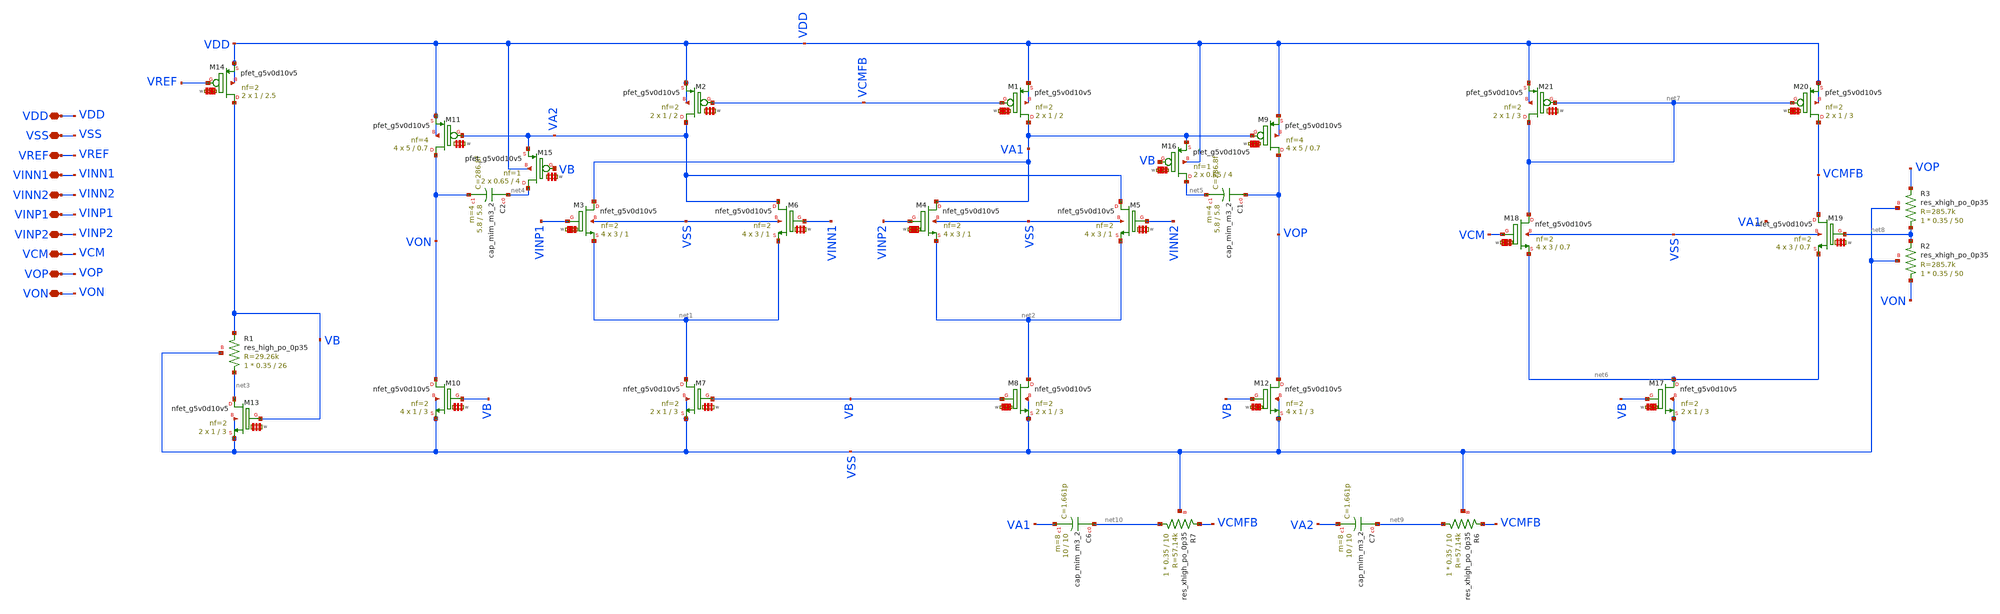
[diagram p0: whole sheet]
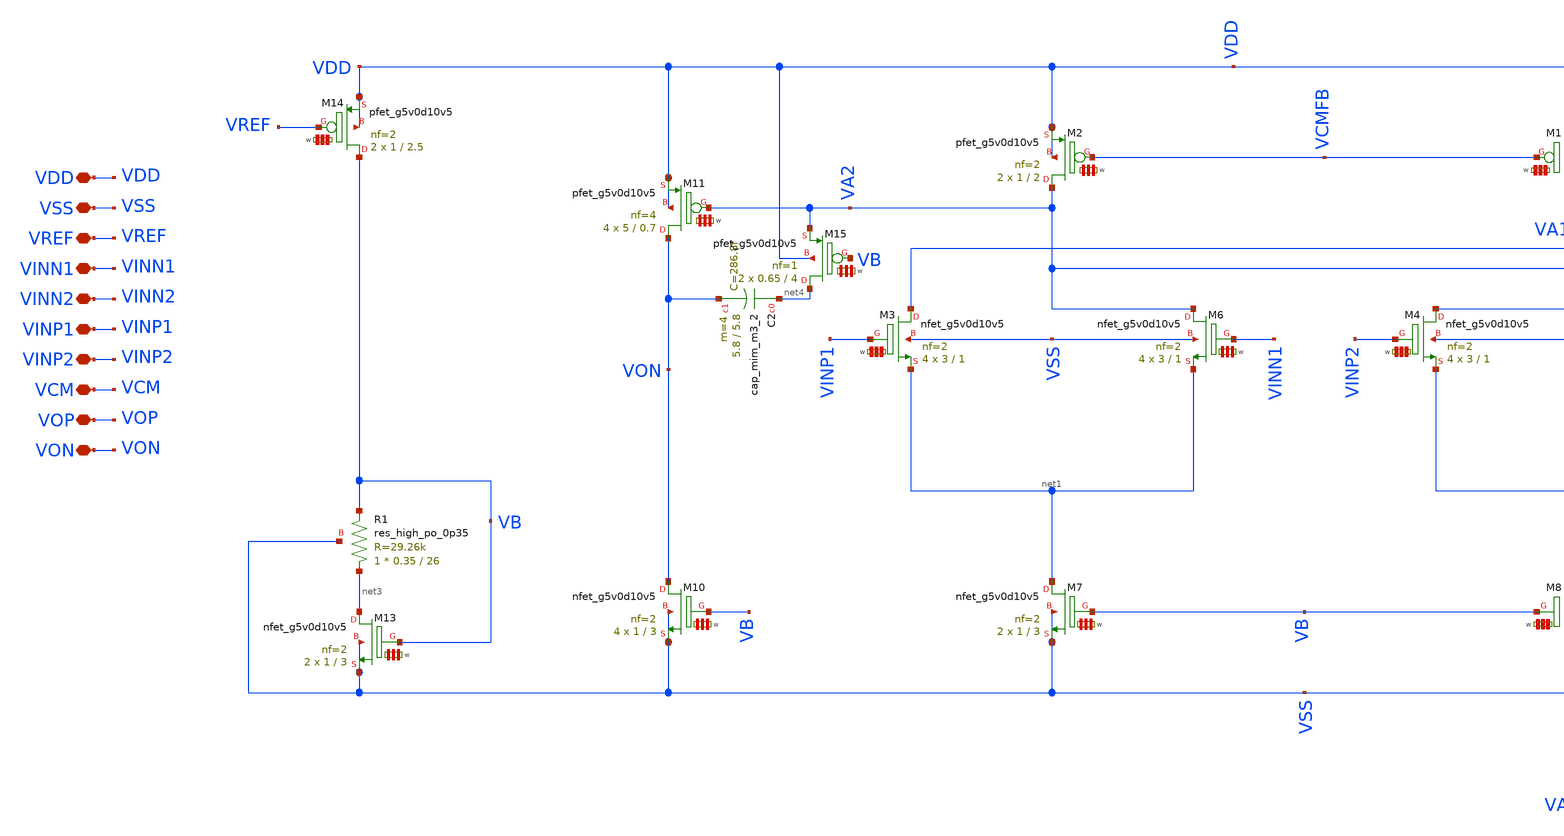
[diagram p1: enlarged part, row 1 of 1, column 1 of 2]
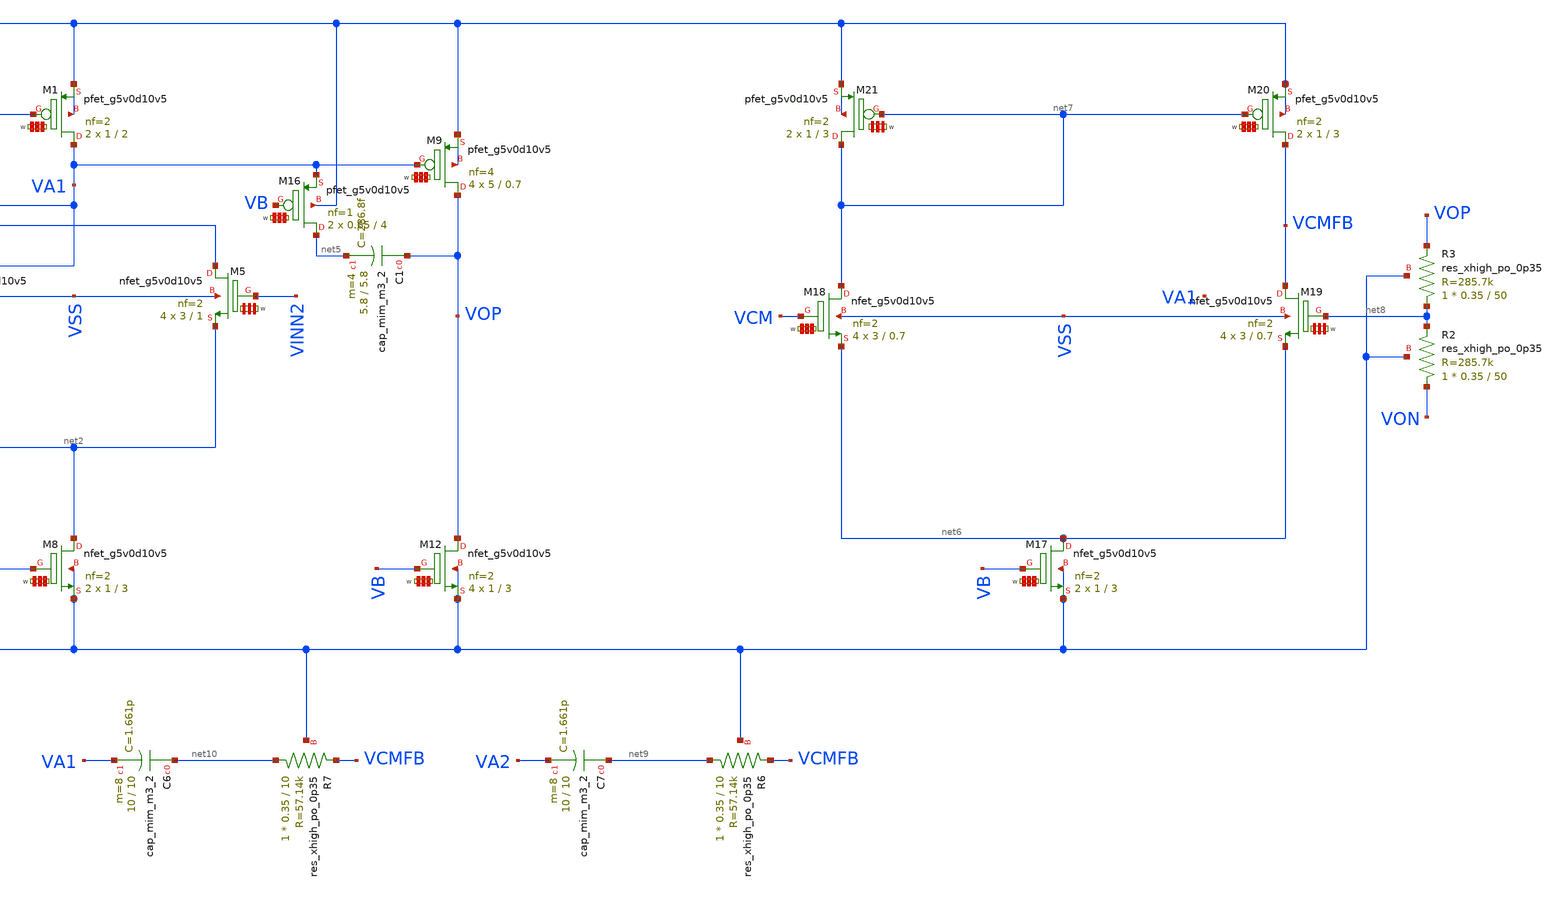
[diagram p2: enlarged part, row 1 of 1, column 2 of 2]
** sch_path: LIB/Sky130A/DDA/DDA002_NMOS_sky130_5V.sch
**.subckt DDA002_NMOS_sky130_5V VDD VSS VREF VINN1 VINN2 VINP1 VINP2 VCM VOP VON
*.iopin VDD
*.iopin VSS
*.iopin VREF
*.iopin VINN1
*.iopin VINN2
*.iopin VINP1
*.iopin VINP2
*.iopin VCM
*.iopin VOP
*.iopin VON
XM2 VA2 VCMFB VDD VDD sky130_fd_pr__pfet_g5v0d10v5 L=2 W='1 * 2 ' nf=2 ad='int((2 + 1)/2) * 1 * 0.29'
+ as='int((2 + 2)/2) * 1 * 0.29' pd='2*int((2 + 1)/2) * (1 + 0.29)' ps='2*int((2 + 2)/2) * (1 + 0.29)'
+ nrd='0.29 / 1 / 2 ' nrs='0.29 / 1 / 2 ' sa=0 sb=0 sd=0 mult=2 m=2
XM3 VA1 VINP1 net1 VSS sky130_fd_pr__nfet_g5v0d10v5 L=1 W='3 * 2 ' nf=2 ad='int((nf+1)/2) * W / nf * 0.29'
+ as='int((nf+2)/2) * W / nf * 0.29' pd='2*int((nf+1)/2) * (W / nf + 0.29)' ps='2*int((nf+2)/2) * (W / nf + 0.29)'
+ nrd='0.29 / W ' nrs='0.29 / W ' sa=0 sb=0 sd=0 mult=4 m=4
XM13 net3 VB VSS VSS sky130_fd_pr__nfet_g5v0d10v5 L=3 W='1 * 2 ' nf=2 ad='int((nf+1)/2) * W / nf * 0.29'
+ as='int((nf+2)/2) * W / nf * 0.29' pd='2*int((nf+1)/2) * (W / nf + 0.29)' ps='2*int((nf+2)/2) * (W / nf + 0.29)'
+ nrd='0.29 / W ' nrs='0.29 / W ' sa=0 sb=0 sd=0 mult=2 m=2
XR1 net3 VB VSS sky130_fd_pr__res_high_po_0p35 L=26 mult=1 m=1
XM14 VB VREF VDD VDD sky130_fd_pr__pfet_g5v0d10v5 L=2.5 W='1 * 2 ' nf=2 ad='int((2 + 1)/2) * 1 * 0.29'
+ as='int((2 + 2)/2) * 1 * 0.29' pd='2*int((2 + 1)/2) * (1 + 0.29)' ps='2*int((2 + 2)/2) * (1 + 0.29)'
+ nrd='0.29 / 1 / 2 ' nrs='0.29 / 1 / 2 ' sa=0 sb=0 sd=0 mult=2 m=2
XM7 net1 VB VSS VSS sky130_fd_pr__nfet_g5v0d10v5 L=3 W='1 * 2 ' nf=2 ad='int((nf+1)/2) * W / nf * 0.29'
+ as='int((nf+2)/2) * W / nf * 0.29' pd='2*int((nf+1)/2) * (W / nf + 0.29)' ps='2*int((nf+2)/2) * (W / nf + 0.29)'
+ nrd='0.29 / W ' nrs='0.29 / W ' sa=0 sb=0 sd=0 mult=2 m=2
XM8 net2 VB VSS VSS sky130_fd_pr__nfet_g5v0d10v5 L=3 W='1 * 2 ' nf=2 ad='int((nf+1)/2) * W / nf * 0.29'
+ as='int((nf+2)/2) * W / nf * 0.29' pd='2*int((nf+1)/2) * (W / nf + 0.29)' ps='2*int((nf+2)/2) * (W / nf + 0.29)'
+ nrd='0.29 / W ' nrs='0.29 / W ' sa=0 sb=0 sd=0 mult=2 m=2
XM10 VON VB VSS VSS sky130_fd_pr__nfet_g5v0d10v5 L=3 W='1 * 2 ' nf=2 ad='int((nf+1)/2) * W / nf * 0.29'
+ as='int((nf+2)/2) * W / nf * 0.29' pd='2*int((nf+1)/2) * (W / nf + 0.29)' ps='2*int((nf+2)/2) * (W / nf + 0.29)'
+ nrd='0.29 / W ' nrs='0.29 / W ' sa=0 sb=0 sd=0 mult=4 m=4
XM12 VOP VB VSS VSS sky130_fd_pr__nfet_g5v0d10v5 L=3 W='1 * 2 ' nf=2 ad='int((nf+1)/2) * W / nf * 0.29'
+ as='int((nf+2)/2) * W / nf * 0.29' pd='2*int((nf+1)/2) * (W / nf + 0.29)' ps='2*int((nf+2)/2) * (W / nf + 0.29)'
+ nrd='0.29 / W ' nrs='0.29 / W ' sa=0 sb=0 sd=0 mult=4 m=4
XM1 VA1 VCMFB VDD VDD sky130_fd_pr__pfet_g5v0d10v5 L=2 W='1 * 2 ' nf=2 ad='int((2 + 1)/2) * 1 * 0.29'
+ as='int((2 + 2)/2) * 1 * 0.29' pd='2*int((2 + 1)/2) * (1 + 0.29)' ps='2*int((2 + 2)/2) * (1 + 0.29)'
+ nrd='0.29 / 1 / 2 ' nrs='0.29 / 1 / 2 ' sa=0 sb=0 sd=0 mult=2 m=2
XM6 VA2 VINN1 net1 VSS sky130_fd_pr__nfet_g5v0d10v5 L=1 W='3 * 2 ' nf=2 ad='int((nf+1)/2) * W / nf * 0.29'
+ as='int((nf+2)/2) * W / nf * 0.29' pd='2*int((nf+1)/2) * (W / nf + 0.29)' ps='2*int((nf+2)/2) * (W / nf + 0.29)'
+ nrd='0.29 / W ' nrs='0.29 / W ' sa=0 sb=0 sd=0 mult=4 m=4
XM5 VA2 VINN2 net2 VSS sky130_fd_pr__nfet_g5v0d10v5 L=1 W='3 * 2 ' nf=2 ad='int((nf+1)/2) * W / nf * 0.29'
+ as='int((nf+2)/2) * W / nf * 0.29' pd='2*int((nf+1)/2) * (W / nf + 0.29)' ps='2*int((nf+2)/2) * (W / nf + 0.29)'
+ nrd='0.29 / W ' nrs='0.29 / W ' sa=0 sb=0 sd=0 mult=4 m=4
XM4 VA1 VINP2 net2 VSS sky130_fd_pr__nfet_g5v0d10v5 L=1 W='3 * 2 ' nf=2 ad='int((nf+1)/2) * W / nf * 0.29'
+ as='int((nf+2)/2) * W / nf * 0.29' pd='2*int((nf+1)/2) * (W / nf + 0.29)' ps='2*int((nf+2)/2) * (W / nf + 0.29)'
+ nrd='0.29 / W ' nrs='0.29 / W ' sa=0 sb=0 sd=0 mult=4 m=4
XM9 VOP VA1 VDD VDD sky130_fd_pr__pfet_g5v0d10v5 L=0.7 W='5 * 4 ' nf=4 ad='int((4 + 1)/2) * 5 * 0.29'
+ as='int((4 + 2)/2) * 5 * 0.29' pd='2*int((4 + 1)/2) * (5 + 0.29)' ps='2*int((4 + 2)/2) * (5 + 0.29)'
+ nrd='0.29 / 5 / 4 ' nrs='0.29 / 5 / 4 ' sa=0 sb=0 sd=0 mult=4 m=4
XM11 VON VA2 VDD VDD sky130_fd_pr__pfet_g5v0d10v5 L=0.7 W='5 * 4 ' nf=4 ad='int((4 + 1)/2) * 5 * 0.29'
+ as='int((4 + 2)/2) * 5 * 0.29' pd='2*int((4 + 1)/2) * (5 + 0.29)' ps='2*int((4 + 2)/2) * (5 + 0.29)'
+ nrd='0.29 / 5 / 4 ' nrs='0.29 / 5 / 4 ' sa=0 sb=0 sd=0 mult=4 m=4
XC2 net4 VON sky130_fd_pr__cap_mim_m3_2 W=5.8 L=5.8 MF=4 m=4
XM15 net4 VB VA2 VDD sky130_fd_pr__pfet_g5v0d10v5 L=4 W='0.65 * 1 ' nf=1 ad='int((1 + 1)/2) * 0.65 * 0.29'
+ as='int((1 + 2)/2) * 0.65 * 0.29' pd='2*int((1 + 1)/2) * (0.65 + 0.29)' ps='2*int((1 + 2)/2) * (0.65 + 0.29)'
+ nrd='0.29 / 0.65 / 1 ' nrs='0.29 / 0.65 / 1 ' sa=0 sb=0 sd=0 mult=2 m=2
XM17 net6 VB VSS VSS sky130_fd_pr__nfet_g5v0d10v5 L=3 W='1 * 2 ' nf=2 ad='int((nf+1)/2) * W / nf * 0.29'
+ as='int((nf+2)/2) * W / nf * 0.29' pd='2*int((nf+1)/2) * (W / nf + 0.29)' ps='2*int((nf+2)/2) * (W / nf + 0.29)'
+ nrd='0.29 / W ' nrs='0.29 / W ' sa=0 sb=0 sd=0 mult=2 m=2
XM18 net7 VCM net6 VSS sky130_fd_pr__nfet_g5v0d10v5 L=0.7 W='3 * 2 ' nf=2 ad='int((nf+1)/2) * W / nf * 0.29'
+ as='int((nf+2)/2) * W / nf * 0.29' pd='2*int((nf+1)/2) * (W / nf + 0.29)' ps='2*int((nf+2)/2) * (W / nf + 0.29)'
+ nrd='0.29 / W ' nrs='0.29 / W ' sa=0 sb=0 sd=0 mult=4 m=4
XM19 VCMFB net8 net6 VSS sky130_fd_pr__nfet_g5v0d10v5 L=0.7 W='3 * 2 ' nf=2 ad='int((nf+1)/2) * W / nf * 0.29'
+ as='int((nf+2)/2) * W / nf * 0.29' pd='2*int((nf+1)/2) * (W / nf + 0.29)' ps='2*int((nf+2)/2) * (W / nf + 0.29)'
+ nrd='0.29 / W ' nrs='0.29 / W ' sa=0 sb=0 sd=0 mult=4 m=4
XM21 net7 net7 VDD VDD sky130_fd_pr__pfet_g5v0d10v5 L=3 W='1 * 2 ' nf=2 ad='int((2 + 1)/2) * 1 * 0.29'
+ as='int((2 + 2)/2) * 1 * 0.29' pd='2*int((2 + 1)/2) * (1 + 0.29)' ps='2*int((2 + 2)/2) * (1 + 0.29)'
+ nrd='0.29 / 1 / 2 ' nrs='0.29 / 1 / 2 ' sa=0 sb=0 sd=0 mult=2 m=2
XM20 VCMFB net7 VDD VDD sky130_fd_pr__pfet_g5v0d10v5 L=3 W='1 * 2 ' nf=2 ad='int((2 + 1)/2) * 1 * 0.29'
+ as='int((2 + 2)/2) * 1 * 0.29' pd='2*int((2 + 1)/2) * (1 + 0.29)' ps='2*int((2 + 2)/2) * (1 + 0.29)'
+ nrd='0.29 / 1 / 2 ' nrs='0.29 / 1 / 2 ' sa=0 sb=0 sd=0 mult=2 m=2
XC6 net10 VA1 sky130_fd_pr__cap_mim_m3_2 W=10 L=10 MF=8 m=8
XR7 net10 VCMFB VSS sky130_fd_pr__res_xhigh_po_0p35 L=10 mult=1 m=1
XC7 net9 VA2 sky130_fd_pr__cap_mim_m3_2 W=10 L=10 MF=8 m=8
XR6 net9 VCMFB VSS sky130_fd_pr__res_xhigh_po_0p35 L=10 mult=1 m=1
XR2 VON net8 VSS sky130_fd_pr__res_xhigh_po_0p35 L=50 mult=1 m=1
XR3 net8 VOP VSS sky130_fd_pr__res_xhigh_po_0p35 L=50 mult=1 m=1
XM16 net5 VB VA1 VDD sky130_fd_pr__pfet_g5v0d10v5 L=4 W='0.65 * 1 ' nf=1 ad='int((1 + 1)/2) * 0.65 * 0.29'
+ as='int((1 + 2)/2) * 0.65 * 0.29' pd='2*int((1 + 1)/2) * (0.65 + 0.29)' ps='2*int((1 + 2)/2) * (0.65 + 0.29)'
+ nrd='0.29 / 0.65 / 1 ' nrs='0.29 / 0.65 / 1 ' sa=0 sb=0 sd=0 mult=2 m=2
XC1 VOP net5 sky130_fd_pr__cap_mim_m3_2 W=5.8 L=5.8 MF=4 m=4
**.ends
.end
